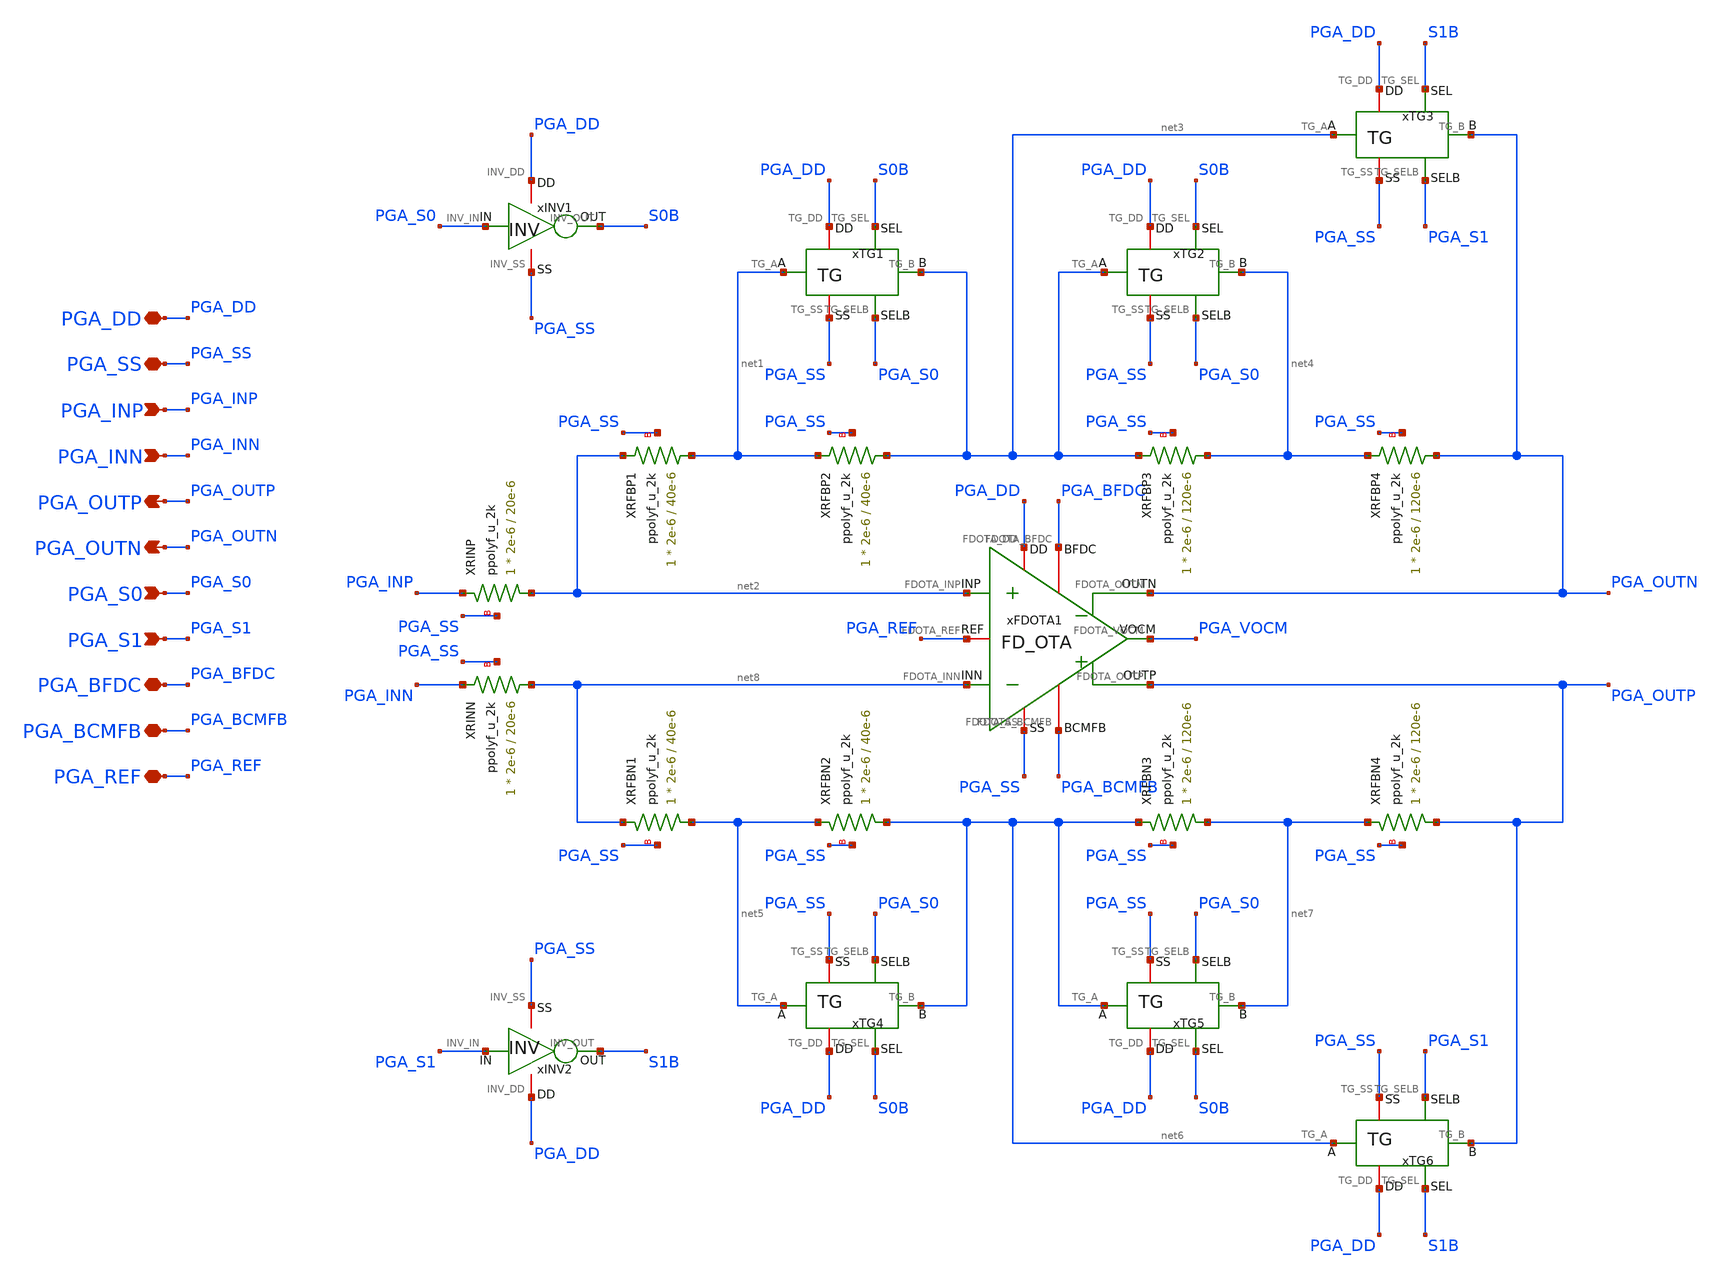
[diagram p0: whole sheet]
** sch_path: Design_Files/IC Design/Schematic/AFE_BLOCKS/PGA/PGA.sch
**.subckt PGA PGA_DD PGA_SS PGA_INP PGA_INN PGA_OUTP PGA_BFDC PGA_OUTN PGA_BCMFB PGA_REF PGA_S0
*+ PGA_S1
*.iopin PGA_DD
*.iopin PGA_SS
*.ipin PGA_INP
*.ipin PGA_INN
*.opin PGA_OUTP
*.iopin PGA_BFDC
*.opin PGA_OUTN
*.iopin PGA_BCMFB
*.iopin PGA_REF
*.ipin PGA_S0
*.ipin PGA_S1
xFDOTA1 PGA_DD PGA_SS net2 net8 PGA_OUTN PGA_BFDC PGA_OUTP PGA_BCMFB PGA_REF PGA_VOCM FD_OTA
xTG1 PGA_DD PGA_SS net1 net3 S0B PGA_S0 TG
xTG3 PGA_DD PGA_SS net3 PGA_OUTN S1B PGA_S1 TG
xINV1 PGA_DD PGA_SS PGA_S0 S0B INV
xTG2 PGA_DD PGA_SS net3 net4 S0B PGA_S0 TG
xTG4 PGA_DD PGA_SS net5 net6 S0B PGA_S0 TG
xTG5 PGA_DD PGA_SS net6 net7 S0B PGA_S0 TG
xINV2 PGA_DD PGA_SS PGA_S1 S1B INV
xTG6 PGA_DD PGA_SS net6 PGA_OUTP S1B PGA_S1 TG
XRINP net2 PGA_INP PGA_SS ppolyf_u_2k r_width=2e-6 r_length=20e-6 m=1
XRINN net8 PGA_INN PGA_SS ppolyf_u_2k r_width=2e-6 r_length=20e-6 m=1
XRFBP1 net1 net2 PGA_SS ppolyf_u_2k r_width=2e-6 r_length=40e-6 m=1
XRFBN1 net5 net8 PGA_SS ppolyf_u_2k r_width=2e-6 r_length=40e-6 m=1
XRFBP2 net3 net1 PGA_SS ppolyf_u_2k r_width=2e-6 r_length=40e-6 m=1
XRFBN2 net6 net5 PGA_SS ppolyf_u_2k r_width=2e-6 r_length=40e-6 m=1
XRFBP3 net4 net3 PGA_SS ppolyf_u_2k r_width=2e-6 r_length=120e-6 m=1
XRFBP4 PGA_OUTN net4 PGA_SS ppolyf_u_2k r_width=2e-6 r_length=120e-6 m=1
XRFBN3 net7 net6 PGA_SS ppolyf_u_2k r_width=2e-6 r_length=120e-6 m=1
XRFBN4 PGA_OUTP net7 PGA_SS ppolyf_u_2k r_width=2e-6 r_length=120e-6 m=1
**.ends
.end
